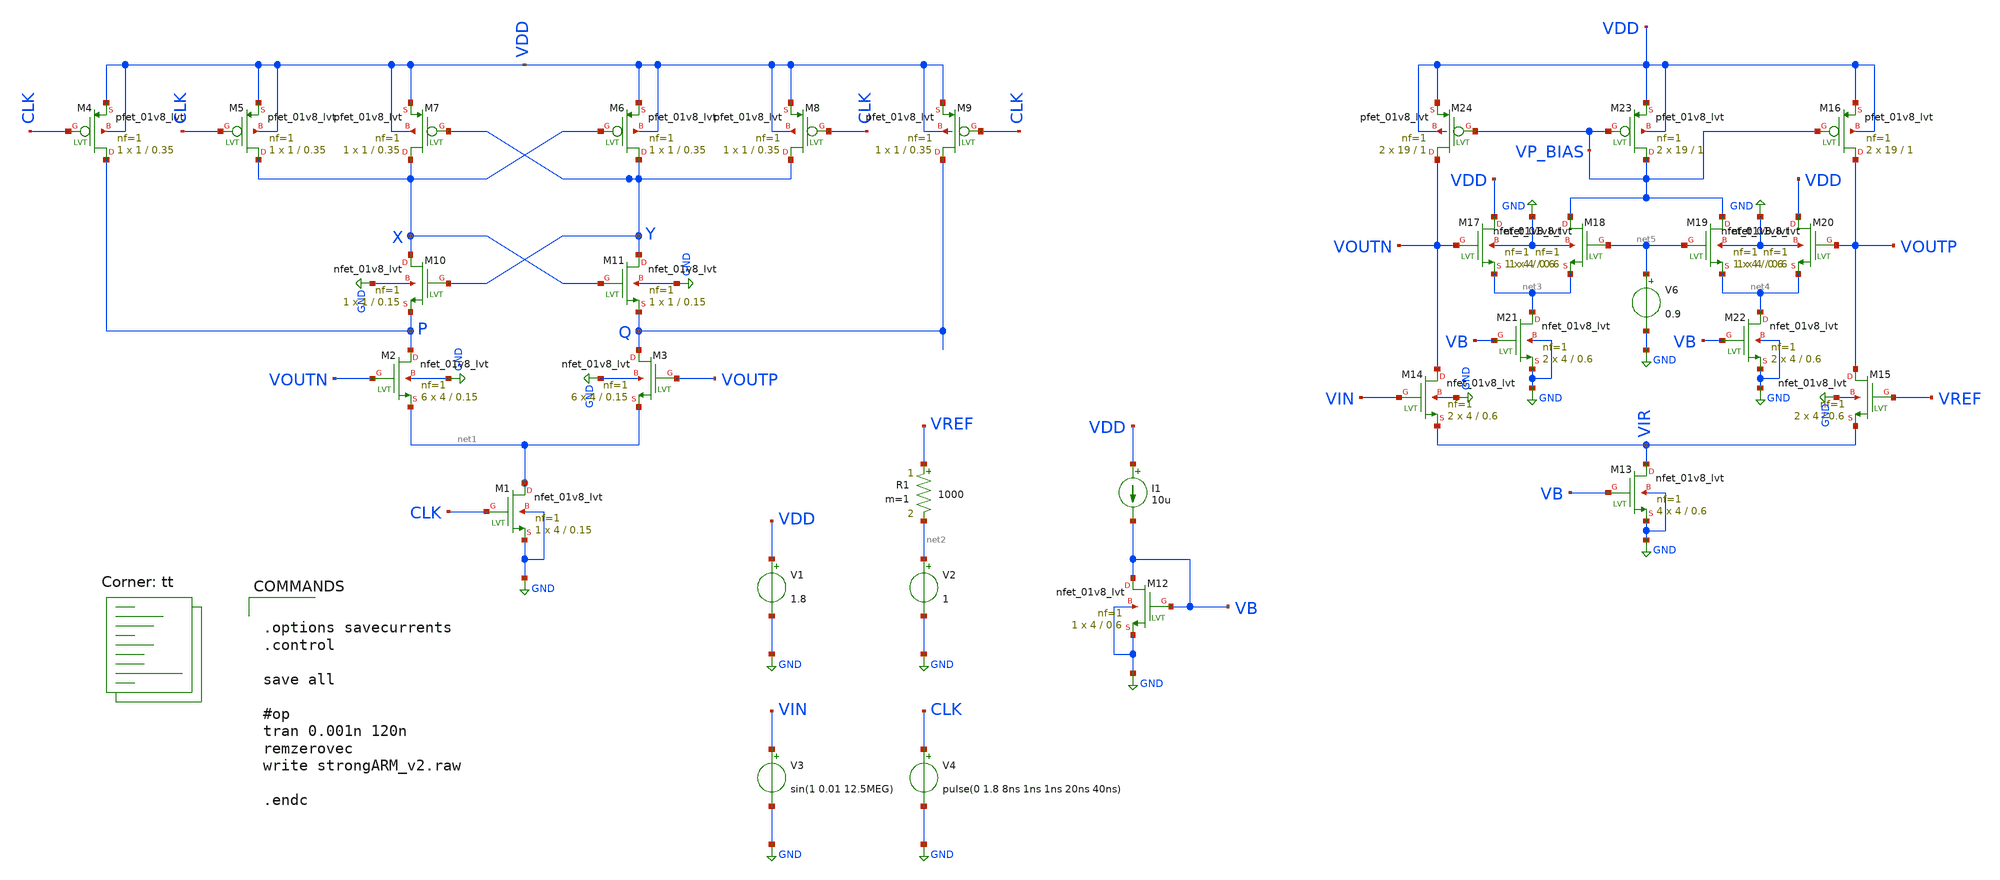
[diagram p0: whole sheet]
** sch_path: strongARM/strongARM_v2.sch
**.subckt strongARM_v2
V1 VDD GND 1.8
V3 VIN GND sin(1 0.01 12.5MEG)
V2 net2 GND 1
V4 CLK GND pulse(0 1.8 8ns 1ns 1ns 20ns 40ns)
XM2 P VOUTN net1 GND sky130_fd_pr__nfet_01v8_lvt L=0.15 W=4 nf=1 ad='int((nf+1)/2) * W/nf * 0.29' as='int((nf+2)/2) * W/nf * 0.29'
+ pd='2*int((nf+1)/2) * (W/nf + 0.29)' ps='2*int((nf+2)/2) * (W/nf + 0.29)' nrd='0.29 / W' nrs='0.29 / W'
+ sa=0 sb=0 sd=0 mult=6 m=6
XM3 Q VOUTP net1 GND sky130_fd_pr__nfet_01v8_lvt L=0.15 W=4 nf=1 ad='int((nf+1)/2) * W/nf * 0.29' as='int((nf+2)/2) * W/nf * 0.29'
+ pd='2*int((nf+1)/2) * (W/nf + 0.29)' ps='2*int((nf+2)/2) * (W/nf + 0.29)' nrd='0.29 / W' nrs='0.29 / W'
+ sa=0 sb=0 sd=0 mult=6 m=6
XM4 P CLK VDD VDD sky130_fd_pr__pfet_01v8_lvt L=0.35 W=1 nf=1 ad='int((nf+1)/2) * W/nf * 0.29' as='int((nf+2)/2) * W/nf * 0.29'
+ pd='2*int((nf+1)/2) * (W/nf + 0.29)' ps='2*int((nf+2)/2) * (W/nf + 0.29)' nrd='0.29 / W' nrs='0.29 / W'
+ sa=0 sb=0 sd=0 mult=1 m=1
XM5 X CLK VDD VDD sky130_fd_pr__pfet_01v8_lvt L=0.35 W=1 nf=1 ad='int((nf+1)/2) * W/nf * 0.29' as='int((nf+2)/2) * W/nf * 0.29'
+ pd='2*int((nf+1)/2) * (W/nf + 0.29)' ps='2*int((nf+2)/2) * (W/nf + 0.29)' nrd='0.29 / W' nrs='0.29 / W'
+ sa=0 sb=0 sd=0 mult=1 m=1
XM6 Y X VDD VDD sky130_fd_pr__pfet_01v8_lvt L=0.35 W=1 nf=1 ad='int((nf+1)/2) * W/nf * 0.29' as='int((nf+2)/2) * W/nf * 0.29'
+ pd='2*int((nf+1)/2) * (W/nf + 0.29)' ps='2*int((nf+2)/2) * (W/nf + 0.29)' nrd='0.29 / W' nrs='0.29 / W'
+ sa=0 sb=0 sd=0 mult=1 m=1
XM7 X Y VDD VDD sky130_fd_pr__pfet_01v8_lvt L=0.35 W=1 nf=1 ad='int((nf+1)/2) * W/nf * 0.29' as='int((nf+2)/2) * W/nf * 0.29'
+ pd='2*int((nf+1)/2) * (W/nf + 0.29)' ps='2*int((nf+2)/2) * (W/nf + 0.29)' nrd='0.29 / W' nrs='0.29 / W'
+ sa=0 sb=0 sd=0 mult=1 m=1
XM8 Y CLK VDD VDD sky130_fd_pr__pfet_01v8_lvt L=0.35 W=1 nf=1 ad='int((nf+1)/2) * W/nf * 0.29' as='int((nf+2)/2) * W/nf * 0.29'
+ pd='2*int((nf+1)/2) * (W/nf + 0.29)' ps='2*int((nf+2)/2) * (W/nf + 0.29)' nrd='0.29 / W' nrs='0.29 / W'
+ sa=0 sb=0 sd=0 mult=1 m=1
XM9 Q CLK VDD VDD sky130_fd_pr__pfet_01v8_lvt L=0.35 W=1 nf=1 ad='int((nf+1)/2) * W/nf * 0.29' as='int((nf+2)/2) * W/nf * 0.29'
+ pd='2*int((nf+1)/2) * (W/nf + 0.29)' ps='2*int((nf+2)/2) * (W/nf + 0.29)' nrd='0.29 / W' nrs='0.29 / W'
+ sa=0 sb=0 sd=0 mult=1 m=1
XM10 X Y P GND sky130_fd_pr__nfet_01v8_lvt L=0.15 W=1 nf=1 ad='int((nf+1)/2) * W/nf * 0.29' as='int((nf+2)/2) * W/nf * 0.29'
+ pd='2*int((nf+1)/2) * (W/nf + 0.29)' ps='2*int((nf+2)/2) * (W/nf + 0.29)' nrd='0.29 / W' nrs='0.29 / W'
+ sa=0 sb=0 sd=0 mult=1 m=1
XM11 Y X Q GND sky130_fd_pr__nfet_01v8_lvt L=0.15 W=1 nf=1 ad='int((nf+1)/2) * W/nf * 0.29' as='int((nf+2)/2) * W/nf * 0.29'
+ pd='2*int((nf+1)/2) * (W/nf + 0.29)' ps='2*int((nf+2)/2) * (W/nf + 0.29)' nrd='0.29 / W' nrs='0.29 / W'
+ sa=0 sb=0 sd=0 mult=1 m=1
XM1 net1 CLK GND GND sky130_fd_pr__nfet_01v8_lvt L=0.15 W=4 nf=1 ad='int((nf+1)/2) * W/nf * 0.29' as='int((nf+2)/2) * W/nf * 0.29'
+ pd='2*int((nf+1)/2) * (W/nf + 0.29)' ps='2*int((nf+2)/2) * (W/nf + 0.29)' nrd='0.29 / W' nrs='0.29 / W'
+ sa=0 sb=0 sd=0 mult=1 m=1
R1 VREF net2 1000 m=1
XM12 VB VB GND GND sky130_fd_pr__nfet_01v8_lvt L=0.6 W=4 nf=1 ad='int((nf+1)/2) * W/nf * 0.29' as='int((nf+2)/2) * W/nf * 0.29'
+ pd='2*int((nf+1)/2) * (W/nf + 0.29)' ps='2*int((nf+2)/2) * (W/nf + 0.29)' nrd='0.29 / W' nrs='0.29 / W'
+ sa=0 sb=0 sd=0 mult=1 m=1
I1 VDD VB 10u
XM13 VIR VB GND GND sky130_fd_pr__nfet_01v8_lvt L=0.6 W=4 nf=1 ad='int((nf+1)/2) * W/nf * 0.29' as='int((nf+2)/2) * W/nf * 0.29'
+ pd='2*int((nf+1)/2) * (W/nf + 0.29)' ps='2*int((nf+2)/2) * (W/nf + 0.29)' nrd='0.29 / W' nrs='0.29 / W'
+ sa=0 sb=0 sd=0 mult=4 m=4
XM14 VOUTN VIN VIR GND sky130_fd_pr__nfet_01v8_lvt L=0.6 W=4 nf=1 ad='int((nf+1)/2) * W/nf * 0.29' as='int((nf+2)/2) * W/nf * 0.29'
+ pd='2*int((nf+1)/2) * (W/nf + 0.29)' ps='2*int((nf+2)/2) * (W/nf + 0.29)' nrd='0.29 / W' nrs='0.29 / W'
+ sa=0 sb=0 sd=0 mult=2 m=2
XM15 VOUTP VREF VIR GND sky130_fd_pr__nfet_01v8_lvt L=0.6 W=4 nf=1 ad='int((nf+1)/2) * W/nf * 0.29' as='int((nf+2)/2) * W/nf * 0.29'
+ pd='2*int((nf+1)/2) * (W/nf + 0.29)' ps='2*int((nf+2)/2) * (W/nf + 0.29)' nrd='0.29 / W' nrs='0.29 / W'
+ sa=0 sb=0 sd=0 mult=2 m=2
XM16 VOUTP VP_BIAS VDD VDD sky130_fd_pr__pfet_01v8_lvt L=1 W=19 nf=1 ad='int((nf+1)/2) * W/nf * 0.29'
+ as='int((nf+2)/2) * W/nf * 0.29' pd='2*int((nf+1)/2) * (W/nf + 0.29)' ps='2*int((nf+2)/2) * (W/nf + 0.29)'
+ nrd='0.29 / W' nrs='0.29 / W' sa=0 sb=0 sd=0 mult=2 m=2
XM17 VDD VOUTN net3 GND sky130_fd_pr__nfet_01v8_lvt L=0.6 W=4 nf=1 ad='int((nf+1)/2) * W/nf * 0.29' as='int((nf+2)/2) * W/nf * 0.29'
+ pd='2*int((nf+1)/2) * (W/nf + 0.29)' ps='2*int((nf+2)/2) * (W/nf + 0.29)' nrd='0.29 / W' nrs='0.29 / W'
+ sa=0 sb=0 sd=0 mult=1 m=1
XM18 VP_BIAS net5 net3 GND sky130_fd_pr__nfet_01v8_lvt L=0.6 W=4 nf=1 ad='int((nf+1)/2) * W/nf * 0.29'
+ as='int((nf+2)/2) * W/nf * 0.29' pd='2*int((nf+1)/2) * (W/nf + 0.29)' ps='2*int((nf+2)/2) * (W/nf + 0.29)'
+ nrd='0.29 / W' nrs='0.29 / W' sa=0 sb=0 sd=0 mult=1 m=1
XM19 VP_BIAS net5 net4 GND sky130_fd_pr__nfet_01v8_lvt L=0.6 W=4 nf=1 ad='int((nf+1)/2) * W/nf * 0.29'
+ as='int((nf+2)/2) * W/nf * 0.29' pd='2*int((nf+1)/2) * (W/nf + 0.29)' ps='2*int((nf+2)/2) * (W/nf + 0.29)'
+ nrd='0.29 / W' nrs='0.29 / W' sa=0 sb=0 sd=0 mult=1 m=1
XM20 VDD VOUTP net4 GND sky130_fd_pr__nfet_01v8_lvt L=0.6 W=4 nf=1 ad='int((nf+1)/2) * W/nf * 0.29' as='int((nf+2)/2) * W/nf * 0.29'
+ pd='2*int((nf+1)/2) * (W/nf + 0.29)' ps='2*int((nf+2)/2) * (W/nf + 0.29)' nrd='0.29 / W' nrs='0.29 / W'
+ sa=0 sb=0 sd=0 mult=1 m=1
XM21 net3 VB GND GND sky130_fd_pr__nfet_01v8_lvt L=0.6 W=4 nf=1 ad='int((nf+1)/2) * W/nf * 0.29' as='int((nf+2)/2) * W/nf * 0.29'
+ pd='2*int((nf+1)/2) * (W/nf + 0.29)' ps='2*int((nf+2)/2) * (W/nf + 0.29)' nrd='0.29 / W' nrs='0.29 / W'
+ sa=0 sb=0 sd=0 mult=2 m=2
XM22 net4 VB GND GND sky130_fd_pr__nfet_01v8_lvt L=0.6 W=4 nf=1 ad='int((nf+1)/2) * W/nf * 0.29' as='int((nf+2)/2) * W/nf * 0.29'
+ pd='2*int((nf+1)/2) * (W/nf + 0.29)' ps='2*int((nf+2)/2) * (W/nf + 0.29)' nrd='0.29 / W' nrs='0.29 / W'
+ sa=0 sb=0 sd=0 mult=2 m=2
XM23 VP_BIAS VP_BIAS VDD VDD sky130_fd_pr__pfet_01v8_lvt L=1 W=19 nf=1 ad='int((nf+1)/2) * W/nf * 0.29'
+ as='int((nf+2)/2) * W/nf * 0.29' pd='2*int((nf+1)/2) * (W/nf + 0.29)' ps='2*int((nf+2)/2) * (W/nf + 0.29)'
+ nrd='0.29 / W' nrs='0.29 / W' sa=0 sb=0 sd=0 mult=2 m=2
V6 net5 GND 0.9
XM24 VOUTN VP_BIAS VDD VDD sky130_fd_pr__pfet_01v8_lvt L=1 W=19 nf=1 ad='int((nf+1)/2) * W/nf * 0.29'
+ as='int((nf+2)/2) * W/nf * 0.29' pd='2*int((nf+1)/2) * (W/nf + 0.29)' ps='2*int((nf+2)/2) * (W/nf + 0.29)'
+ nrd='0.29 / W' nrs='0.29 / W' sa=0 sb=0 sd=0 mult=2 m=2
**** begin user architecture code
.lib $::SKYWATER_MODELS/sky130.lib.spice tt


.options savecurrents
.control

save all

#op
tran 0.001n 120n
remzerovec
write strongARM_v2.raw

.endc


**** end user architecture code
**.ends
.GLOBAL GND
.end
